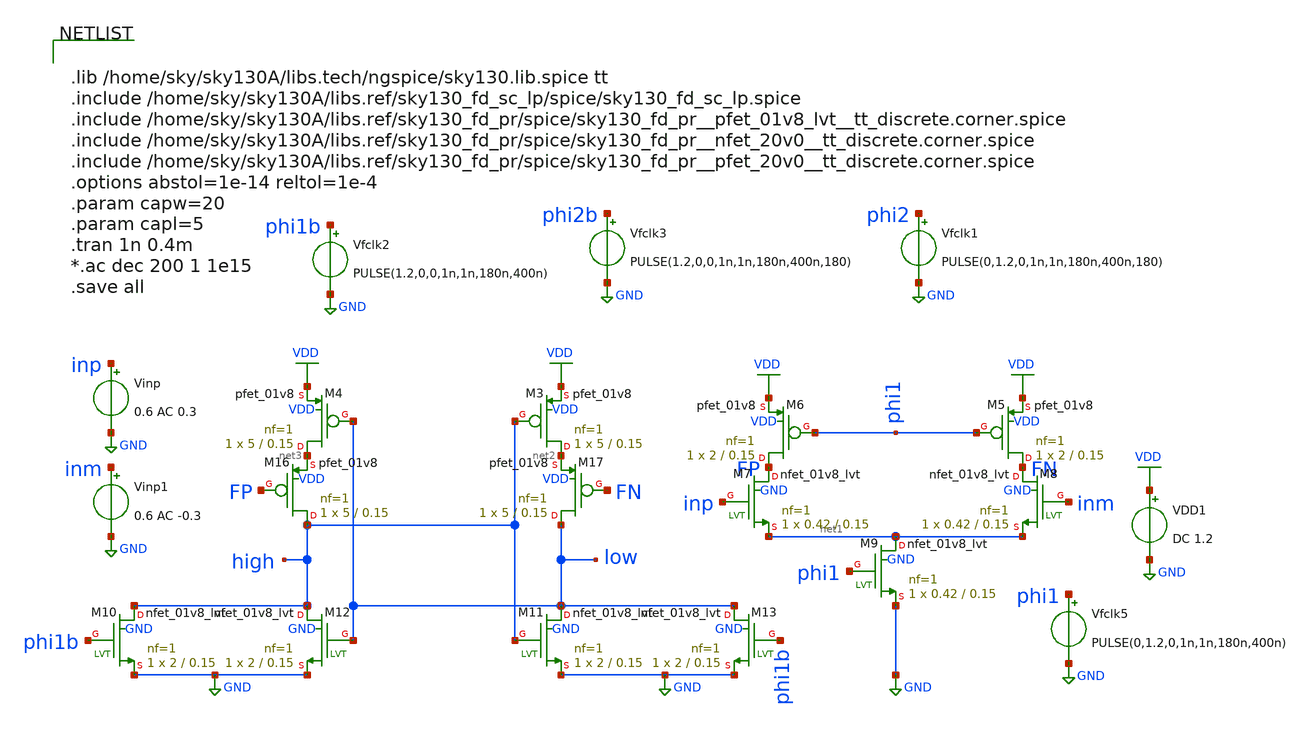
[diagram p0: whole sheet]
** sch_path: xschem/comparator_latest/HW1_264A.sch
**.subckt HW1_264A
Vinp inp GND 0.6 AC 0.3
XM3 net2 high VDD VDD sky130_fd_pr__pfet_01v8 L=0.15 W=5 nf=1 ad='int((nf+1)/2) * W/nf * 0.29' as='int((nf+2)/2) * W/nf * 0.29'
+ pd='2*int((nf+1)/2) * (W/nf + 0.29)' ps='2*int((nf+2)/2) * (W/nf + 0.29)' nrd='0.29 / W' nrs='0.29 / W'
+ sa=0 sb=0 sd=0 mult=1 m=1
XM4 net3 low VDD VDD sky130_fd_pr__pfet_01v8 L=0.15 W=5 nf=1 ad='int((nf+1)/2) * W/nf * 0.29' as='int((nf+2)/2) * W/nf * 0.29'
+ pd='2*int((nf+1)/2) * (W/nf + 0.29)' ps='2*int((nf+2)/2) * (W/nf + 0.29)' nrd='0.29 / W' nrs='0.29 / W'
+ sa=0 sb=0 sd=0 mult=1 m=1
XM16 high FP net3 VDD sky130_fd_pr__pfet_01v8 L=0.15 W=5 nf=1 ad='int((nf+1)/2) * W/nf * 0.29' as='int((nf+2)/2) * W/nf * 0.29'
+ pd='2*int((nf+1)/2) * (W/nf + 0.29)' ps='2*int((nf+2)/2) * (W/nf + 0.29)' nrd='0.29 / W' nrs='0.29 / W'
+ sa=0 sb=0 sd=0 mult=1 m=1
XM17 low FN net2 VDD sky130_fd_pr__pfet_01v8 L=0.15 W=5 nf=1 ad='int((nf+1)/2) * W/nf * 0.29' as='int((nf+2)/2) * W/nf * 0.29'
+ pd='2*int((nf+1)/2) * (W/nf + 0.29)' ps='2*int((nf+2)/2) * (W/nf + 0.29)' nrd='0.29 / W' nrs='0.29 / W'
+ sa=0 sb=0 sd=0 mult=1 m=1
XM5 FN phi1 VDD VDD sky130_fd_pr__pfet_01v8 L=0.15 W=2 nf=1 ad='int((nf+1)/2) * W/nf * 0.29' as='int((nf+2)/2) * W/nf * 0.29'
+ pd='2*int((nf+1)/2) * (W/nf + 0.29)' ps='2*int((nf+2)/2) * (W/nf + 0.29)' nrd='0.29 / W' nrs='0.29 / W'
+ sa=0 sb=0 sd=0 mult=1 m=1
XM6 FP phi1 VDD VDD sky130_fd_pr__pfet_01v8 L=0.15 W=2 nf=1 ad='int((nf+1)/2) * W/nf * 0.29' as='int((nf+2)/2) * W/nf * 0.29'
+ pd='2*int((nf+1)/2) * (W/nf + 0.29)' ps='2*int((nf+2)/2) * (W/nf + 0.29)' nrd='0.29 / W' nrs='0.29 / W'
+ sa=0 sb=0 sd=0 mult=1 m=1
XM7 FP inp net1 GND sky130_fd_pr__nfet_01v8_lvt L=0.15 W=0.42 nf=1 ad='int((nf+1)/2) * W/nf * 0.29' as='int((nf+2)/2) * W/nf * 0.29'
+ pd='2*int((nf+1)/2) * (W/nf + 0.29)' ps='2*int((nf+2)/2) * (W/nf + 0.29)' nrd='0.29 / W' nrs='0.29 / W'
+ sa=0 sb=0 sd=0 mult=1 m=1
XM8 FN inm net1 GND sky130_fd_pr__nfet_01v8_lvt L=0.15 W=0.42 nf=1 ad='int((nf+1)/2) * W/nf * 0.29' as='int((nf+2)/2) * W/nf * 0.29'
+ pd='2*int((nf+1)/2) * (W/nf + 0.29)' ps='2*int((nf+2)/2) * (W/nf + 0.29)' nrd='0.29 / W' nrs='0.29 / W'
+ sa=0 sb=0 sd=0 mult=1 m=1
XM9 net1 phi1 GND GND sky130_fd_pr__nfet_01v8_lvt L=0.15 W=0.42 nf=1 ad='int((nf+1)/2) * W/nf * 0.29'
+ as='int((nf+2)/2) * W/nf * 0.29' pd='2*int((nf+1)/2) * (W/nf + 0.29)' ps='2*int((nf+2)/2) * (W/nf + 0.29)'
+ nrd='0.29 / W' nrs='0.29 / W' sa=0 sb=0 sd=0 mult=1 m=1
XM10 high phi1b GND GND sky130_fd_pr__nfet_01v8_lvt L=0.15 W=2 nf=1 ad='int((nf+1)/2) * W/nf * 0.29'
+ as='int((nf+2)/2) * W/nf * 0.29' pd='2*int((nf+1)/2) * (W/nf + 0.29)' ps='2*int((nf+2)/2) * (W/nf + 0.29)'
+ nrd='0.29 / W' nrs='0.29 / W' sa=0 sb=0 sd=0 mult=1 m=1
XM11 low high GND GND sky130_fd_pr__nfet_01v8_lvt L=0.15 W=2 nf=1 ad='int((nf+1)/2) * W/nf * 0.29' as='int((nf+2)/2) * W/nf * 0.29'
+ pd='2*int((nf+1)/2) * (W/nf + 0.29)' ps='2*int((nf+2)/2) * (W/nf + 0.29)' nrd='0.29 / W' nrs='0.29 / W'
+ sa=0 sb=0 sd=0 mult=1 m=1
XM12 high low GND GND sky130_fd_pr__nfet_01v8_lvt L=0.15 W=2 nf=1 ad='int((nf+1)/2) * W/nf * 0.29' as='int((nf+2)/2) * W/nf * 0.29'
+ pd='2*int((nf+1)/2) * (W/nf + 0.29)' ps='2*int((nf+2)/2) * (W/nf + 0.29)' nrd='0.29 / W' nrs='0.29 / W'
+ sa=0 sb=0 sd=0 mult=1 m=1
XM13 low phi1b GND GND sky130_fd_pr__nfet_01v8_lvt L=0.15 W=2 nf=1 ad='int((nf+1)/2) * W/nf * 0.29' as='int((nf+2)/2) * W/nf * 0.29'
+ pd='2*int((nf+1)/2) * (W/nf + 0.29)' ps='2*int((nf+2)/2) * (W/nf + 0.29)' nrd='0.29 / W' nrs='0.29 / W'
+ sa=0 sb=0 sd=0 mult=1 m=1
VDD1 VDD GND DC 1.2
Vfclk1 phi2 GND PULSE(0,1.2,0,1n,1n,180n,400n,180)
Vfclk2 phi1b GND PULSE(1.2,0,0,1n,1n,180n,400n)
Vfclk3 phi2b GND PULSE(1.2,0,0,1n,1n,180n,400n,180)
Vfclk5 phi1 GND PULSE(0,1.2,0,1n,1n,180n,400n)
Vinp1 inm GND 0.6 AC -0.3
**** begin user architecture code


.lib /home/sky/sky130A/libs.tech/ngspice/sky130.lib.spice tt
.include /home/sky/sky130A/libs.ref/sky130_fd_sc_lp/spice/sky130_fd_sc_lp.spice
.include /home/sky/sky130A/libs.ref/sky130_fd_pr/spice/sky130_fd_pr__pfet_01v8_lvt__tt_discrete.corner.spice
.include /home/sky/sky130A/libs.ref/sky130_fd_pr/spice/sky130_fd_pr__nfet_20v0__tt_discrete.corner.spice
.include /home/sky/sky130A/libs.ref/sky130_fd_pr/spice/sky130_fd_pr__pfet_20v0__tt_discrete.corner.spice
.options abstol=1e-14 reltol=1e-4
.param capw=20
.param capl=5
.tran 1n 0.4m
*.ac dec 200 1 1e15
.save all


**** end user architecture code
**.ends
.GLOBAL GND
.GLOBAL VDD
.end
